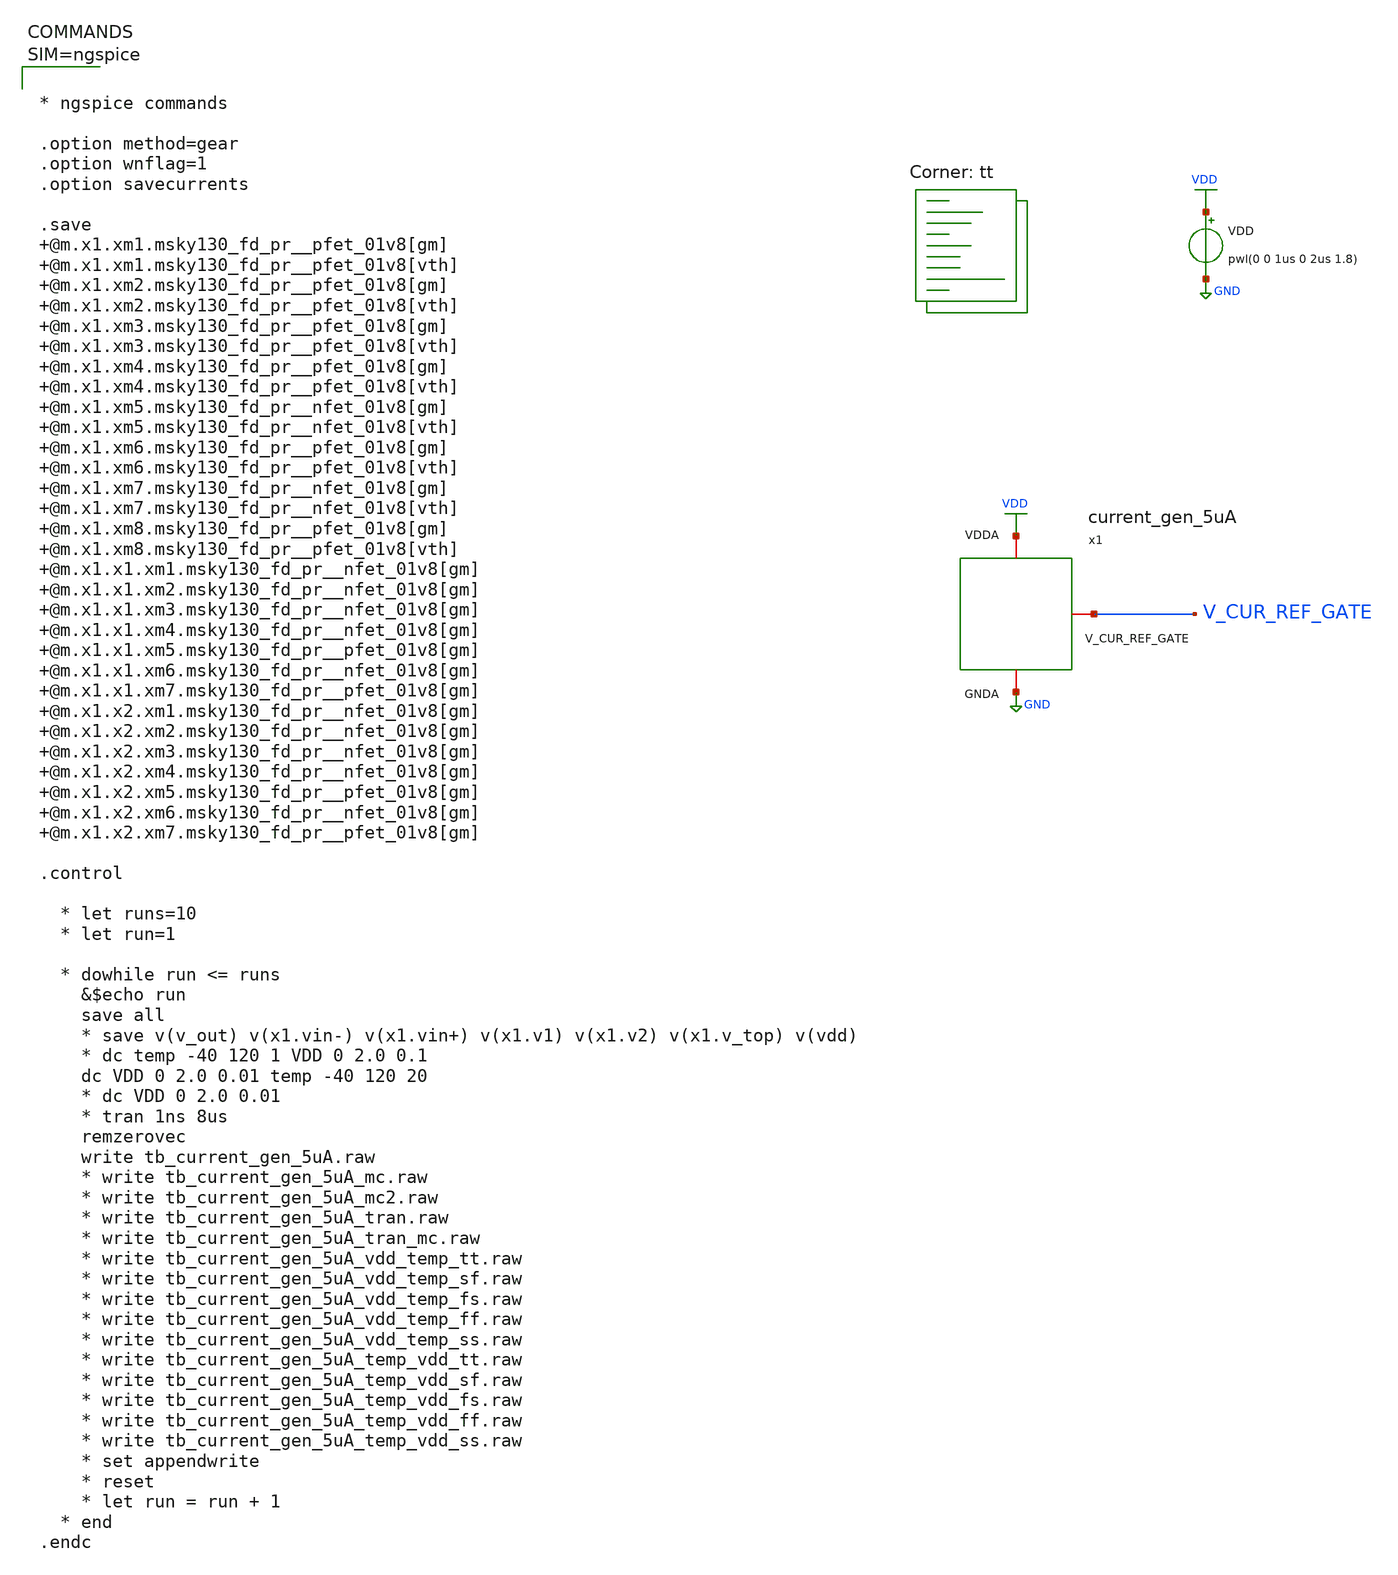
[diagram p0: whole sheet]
** sch_path: projects/bandgapref/xschem_ngspice/new_files/tb_current_gen_5uA.sch
**.subckt tb_current_gen_5uA
VDD VDD GND pwl(0 0 1us 0 2us 1.8)
x1 VDD V_CUR_REF_GATE GND current_gen_5uA
**** begin user architecture code
.lib $::SKYWATER_MODELS/sky130.lib.spice tt



* ngspice commands

.option method=gear
.option wnflag=1
.option savecurrents

.save @m.x1.xm1.msky130_fd_pr__pfet_01v8[gm] @m.x1.xm1.msky130_fd_pr__pfet_01v8[vth] @m.x1.xm2.msky130_fd_pr__pfet_01v8[gm] @m.x1.xm2.msky130_fd_pr__pfet_01v8[vth] @m.x1.xm3.msky130_fd_pr__pfet_01v8[gm] @m.x1.xm3.msky130_fd_pr__pfet_01v8[vth] @m.x1.xm4.msky130_fd_pr__pfet_01v8[gm] @m.x1.xm4.msky130_fd_pr__pfet_01v8[vth] @m.x1.xm5.msky130_fd_pr__nfet_01v8[gm] @m.x1.xm5.msky130_fd_pr__nfet_01v8[vth] @m.x1.xm6.msky130_fd_pr__pfet_01v8[gm] @m.x1.xm6.msky130_fd_pr__pfet_01v8[vth] @m.x1.xm7.msky130_fd_pr__nfet_01v8[gm] @m.x1.xm7.msky130_fd_pr__nfet_01v8[vth] @m.x1.xm8.msky130_fd_pr__pfet_01v8[gm] @m.x1.xm8.msky130_fd_pr__pfet_01v8[vth] @m.x1.x1.xm1.msky130_fd_pr__nfet_01v8[gm] @m.x1.x1.xm2.msky130_fd_pr__nfet_01v8[gm] @m.x1.x1.xm3.msky130_fd_pr__nfet_01v8[gm] @m.x1.x1.xm4.msky130_fd_pr__nfet_01v8[gm] @m.x1.x1.xm5.msky130_fd_pr__pfet_01v8[gm] @m.x1.x1.xm6.msky130_fd_pr__nfet_01v8[gm] @m.x1.x1.xm7.msky130_fd_pr__pfet_01v8[gm] @m.x1.x2.xm1.msky130_fd_pr__nfet_01v8[gm] @m.x1.x2.xm2.msky130_fd_pr__nfet_01v8[gm] @m.x1.x2.xm3.msky130_fd_pr__nfet_01v8[gm] @m.x1.x2.xm4.msky130_fd_pr__nfet_01v8[gm] @m.x1.x2.xm5.msky130_fd_pr__pfet_01v8[gm] @m.x1.x2.xm6.msky130_fd_pr__nfet_01v8[gm] @m.x1.x2.xm7.msky130_fd_pr__pfet_01v8[gm]

.control

  * let runs=10
  * let run=1

  * dowhile run <= runs
    &$echo run
    save all
    * save v(v_out) v(x1.vin-) v(x1.vin+) v(x1.v1) v(x1.v2) v(x1.v_top) v(vdd)
    * dc temp -40 120 1 VDD 0 2.0 0.1
    dc VDD 0 2.0 0.01 temp -40 120 20
    * dc VDD 0 2.0 0.01
    * tran 1ns 8us
    remzerovec
    write tb_current_gen_5uA.raw
    * write tb_current_gen_5uA_mc.raw
    * write tb_current_gen_5uA_mc2.raw
    * write tb_current_gen_5uA_tran.raw
    * write tb_current_gen_5uA_tran_mc.raw
    * write tb_current_gen_5uA_vdd_temp_tt.raw
    * write tb_current_gen_5uA_vdd_temp_sf.raw
    * write tb_current_gen_5uA_vdd_temp_fs.raw
    * write tb_current_gen_5uA_vdd_temp_ff.raw
    * write tb_current_gen_5uA_vdd_temp_ss.raw
    * write tb_current_gen_5uA_temp_vdd_tt.raw
    * write tb_current_gen_5uA_temp_vdd_sf.raw
    * write tb_current_gen_5uA_temp_vdd_fs.raw
    * write tb_current_gen_5uA_temp_vdd_ff.raw
    * write tb_current_gen_5uA_temp_vdd_ss.raw
    * set appendwrite
    * reset
    * let run = run + 1
  * end
.endc




**** end user architecture code
**.ends

* expanding   symbol:  current_gen_5uA.sym # of pins=3
** sym_path: projects/bandgapref/xschem_ngspice/new_files/current_gen_5uA.sym
** sch_path: projects/bandgapref/xschem_ngspice/new_files/current_gen_5uA.sch
.subckt current_gen_5uA VDDA V_CUR_REF_GATE GNDA
*.iopin VDDA
*.iopin GNDA
*.opin V_CUR_REF_GATE
XQ1 GNDA GNDA Vin- sky130_fd_pr__pnp_05v5_W3p40L3p40 m=1
XQ2 GNDA GNDA Vbe2 sky130_fd_pr__pnp_05v5_W3p40L3p40 m=8
XM1 Vin- V_TOP VDDA VDDA sky130_fd_pr__pfet_01v8 L=0.3 W=10 nf=1 ad='int((nf+1)/2) * W/nf * 0.29' as='int((nf+2)/2) * W/nf * 0.29'
+ pd='2*int((nf+1)/2) * (W/nf + 0.29)' ps='2*int((nf+2)/2) * (W/nf + 0.29)' nrd='0.29 / W' nrs='0.29 / W'
+ sa=0 sb=0 sd=0 mult=1 m=1
XM2 Vin+ V_TOP VDDA VDDA sky130_fd_pr__pfet_01v8 L=0.3 W=10 nf=1 ad='int((nf+1)/2) * W/nf * 0.29' as='int((nf+2)/2) * W/nf * 0.29'
+ pd='2*int((nf+1)/2) * (W/nf + 0.29)' ps='2*int((nf+2)/2) * (W/nf + 0.29)' nrd='0.29 / W' nrs='0.29 / W'
+ sa=0 sb=0 sd=0 mult=1 m=1
XM3 V_REF V_TOP VDDA VDDA sky130_fd_pr__pfet_01v8 L=0.3 W=10 nf=1 ad='int((nf+1)/2) * W/nf * 0.29' as='int((nf+2)/2) * W/nf * 0.29'
+ pd='2*int((nf+1)/2) * (W/nf + 0.29)' ps='2*int((nf+2)/2) * (W/nf + 0.29)' nrd='0.29 / W' nrs='0.29 / W'
+ sa=0 sb=0 sd=0 mult=1 m=1
XR1 Vbe2 Vin+ GNDA sky130_fd_pr__res_xhigh_po_0p35 L=3.87 mult=1 m=1
XR2 GNDA Vin+ GNDA sky130_fd_pr__res_xhigh_po_0p35 L=32 mult=1 m=1
XR3 GNDA Vin- GNDA sky130_fd_pr__res_xhigh_po_0p35 L=32 mult=1 m=1
XR4 GNDA V_REF GNDA sky130_fd_pr__res_xhigh_po_0p35 L=32 mult=1 m=1
XM5 start_up start_up start_up_nfet1 start_up_nfet1 sky130_fd_pr__nfet_01v8 L=10 W=1 nf=1 ad='int((nf+1)/2) * W/nf * 0.29'
+ as='int((nf+2)/2) * W/nf * 0.29' pd='2*int((nf+1)/2) * (W/nf + 0.29)' ps='2*int((nf+2)/2) * (W/nf + 0.29)'
+ nrd='0.29 / W' nrs='0.29 / W' sa=0 sb=0 sd=0 mult=1 m=1
XM6 start_up V_TOP VDDA VDDA sky130_fd_pr__pfet_01v8 L=0.3 W=10 nf=1 ad='int((nf+1)/2) * W/nf * 0.29'
+ as='int((nf+2)/2) * W/nf * 0.29' pd='2*int((nf+1)/2) * (W/nf + 0.29)' ps='2*int((nf+2)/2) * (W/nf + 0.29)'
+ nrd='0.29 / W' nrs='0.29 / W' sa=0 sb=0 sd=0 mult=1 m=1
XM4 Vin- start_up V_TOP VDDA sky130_fd_pr__pfet_01v8 L=0.15 W=2 nf=1 ad='int((nf+1)/2) * W/nf * 0.29'
+ as='int((nf+2)/2) * W/nf * 0.29' pd='2*int((nf+1)/2) * (W/nf + 0.29)' ps='2*int((nf+2)/2) * (W/nf + 0.29)'
+ nrd='0.29 / W' nrs='0.29 / W' sa=0 sb=0 sd=0 mult=1 m=1
x1 VDDA V_TOP Vin- Vin+ GNDA opamp_bandgap_2
XM7 start_up_nfet1 start_up_nfet1 GNDA GNDA sky130_fd_pr__nfet_01v8 L=10 W=1 nf=1 ad='int((nf+1)/2) * W/nf * 0.29'
+ as='int((nf+2)/2) * W/nf * 0.29' pd='2*int((nf+1)/2) * (W/nf + 0.29)' ps='2*int((nf+2)/2) * (W/nf + 0.29)'
+ nrd='0.29 / W' nrs='0.29 / W' sa=0 sb=0 sd=0 mult=1 m=1
x2 VDD V_CUR_REF_GATE V_REF V_CUR_REF_REG GND opamp_bandgap_2
XR6 GNDA V_CUR_REF_REG GND sky130_fd_pr__res_xhigh_po_0p35 L=32 mult=1 m=1
XM8 V_CUR_REF_REG V_CUR_REF_GATE VDDA VDDA sky130_fd_pr__pfet_01v8 L=0.3 W=10 nf=1 ad='int((nf+1)/2) * W/nf * 0.29'
+ as='int((nf+2)/2) * W/nf * 0.29' pd='2*int((nf+1)/2) * (W/nf + 0.29)' ps='2*int((nf+2)/2) * (W/nf + 0.29)'
+ nrd='0.29 / W' nrs='0.29 / W' sa=0 sb=0 sd=0 mult=1 m=1
.ends


* expanding   symbol:  opamp_bandgap_2.sym # of pins=5
** sym_path: projects/bandgapref/xschem_ngspice/new_files/opamp_bandgap_2.sym
** sch_path: projects/bandgapref/xschem_ngspice/new_files/opamp_bandgap_2.sch
.subckt opamp_bandgap_2 VDDA Vout Vin- Vin+ GNDA
*.ipin Vin+
*.opin Vout
*.ipin Vin-
*.ipin GNDA
*.ipin VDDA
XM1 V_p VDDA GNDA GNDA sky130_fd_pr__nfet_01v8 L=10 W=5 nf=1 ad='int((nf+1)/2) * W/nf * 0.29' as='int((nf+2)/2) * W/nf * 0.29'
+ pd='2*int((nf+1)/2) * (W/nf + 0.29)' ps='2*int((nf+2)/2) * (W/nf + 0.29)' nrd='0.29 / W' nrs='0.29 / W'
+ sa=0 sb=0 sd=0 mult=1 m=1
XM2 V_mirror Vin- V_p GNDA sky130_fd_pr__nfet_01v8 L=0.2 W=5 nf=1 ad='int((nf+1)/2) * W/nf * 0.29' as='int((nf+2)/2) * W/nf * 0.29'
+ pd='2*int((nf+1)/2) * (W/nf + 0.29)' ps='2*int((nf+2)/2) * (W/nf + 0.29)' nrd='0.29 / W' nrs='0.29 / W'
+ sa=0 sb=0 sd=0 mult=1 m=1
XM3 1st_Vout Vin+ V_p GNDA sky130_fd_pr__nfet_01v8 L=0.2 W=5 nf=1 ad='int((nf+1)/2) * W/nf * 0.29' as='int((nf+2)/2) * W/nf * 0.29'
+ pd='2*int((nf+1)/2) * (W/nf + 0.29)' ps='2*int((nf+2)/2) * (W/nf + 0.29)' nrd='0.29 / W' nrs='0.29 / W'
+ sa=0 sb=0 sd=0 mult=1 m=1
XM5 V_mirror V_mirror VDDA VDDA sky130_fd_pr__pfet_01v8 L=0.2 W=10 nf=2 ad='int((nf+1)/2) * W/nf * 0.29'
+ as='int((nf+2)/2) * W/nf * 0.29' pd='2*int((nf+1)/2) * (W/nf + 0.29)' ps='2*int((nf+2)/2) * (W/nf + 0.29)'
+ nrd='0.29 / W' nrs='0.29 / W' sa=0 sb=0 sd=0 mult=1 m=1
XM6 1st_Vout V_mirror VDDA VDDA sky130_fd_pr__pfet_01v8 L=0.2 W=10 nf=2 ad='int((nf+1)/2) * W/nf * 0.29'
+ as='int((nf+2)/2) * W/nf * 0.29' pd='2*int((nf+1)/2) * (W/nf + 0.29)' ps='2*int((nf+2)/2) * (W/nf + 0.29)'
+ nrd='0.29 / W' nrs='0.29 / W' sa=0 sb=0 sd=0 mult=1 m=1
XM4 Vout VDDA GNDA GNDA sky130_fd_pr__nfet_01v8 L=10 W=5 nf=1 ad='int((nf+1)/2) * W/nf * 0.29' as='int((nf+2)/2) * W/nf * 0.29'
+ pd='2*int((nf+1)/2) * (W/nf + 0.29)' ps='2*int((nf+2)/2) * (W/nf + 0.29)' nrd='0.29 / W' nrs='0.29 / W'
+ sa=0 sb=0 sd=0 mult=1 m=1
XM7 Vout 1st_Vout VDDA VDDA sky130_fd_pr__pfet_01v8 L=0.2 W=10 nf=2 ad='int((nf+1)/2) * W/nf * 0.29'
+ as='int((nf+2)/2) * W/nf * 0.29' pd='2*int((nf+1)/2) * (W/nf + 0.29)' ps='2*int((nf+2)/2) * (W/nf + 0.29)'
+ nrd='0.29 / W' nrs='0.29 / W' sa=0 sb=0 sd=0 mult=1 m=1
.ends

.GLOBAL GND
.GLOBAL VDD
.end
